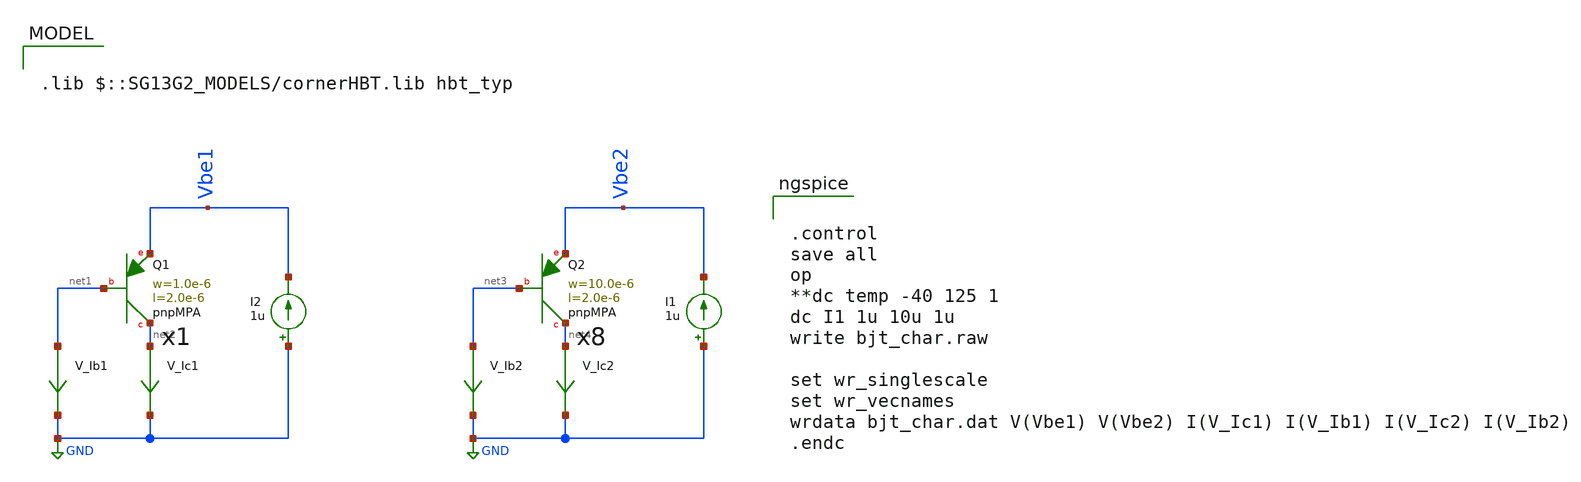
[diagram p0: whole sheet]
** sch_path: transistor-characterisation/bjt_char.sch
**.subckt bjt_char
XQ1 net2 net1 Vbe1 pnpMPA a=2p p=6u m=1
I2 GND Vbe1 1u
V_Ic1 net2 GND 0
.save i(v_ic1)
V_Ib1 net1 GND 0
.save i(v_ib1)
XQ2 net4 net3 Vbe2 pnpMPA a=20p p=24u m=8
I1 GND Vbe2 1u
V_Ic2 net4 GND 0
.save i(v_ic2)
V_Ib2 net3 GND 0
.save i(v_ib2)
**** begin user architecture code

.lib $::SG13G2_MODELS/cornerHBT.lib hbt_typ



.control
save all
op
**dc temp -40 125 1
dc I1 1u 10u 1u
write bjt_char.raw

set wr_singlescale
set wr_vecnames
wrdata bjt_char.dat V(Vbe1) V(Vbe2) I(V_Ic1) I(V_Ib1) I(V_Ic2) I(V_Ib2)
.endc


**** end user architecture code
**.ends
.GLOBAL GND
.end
